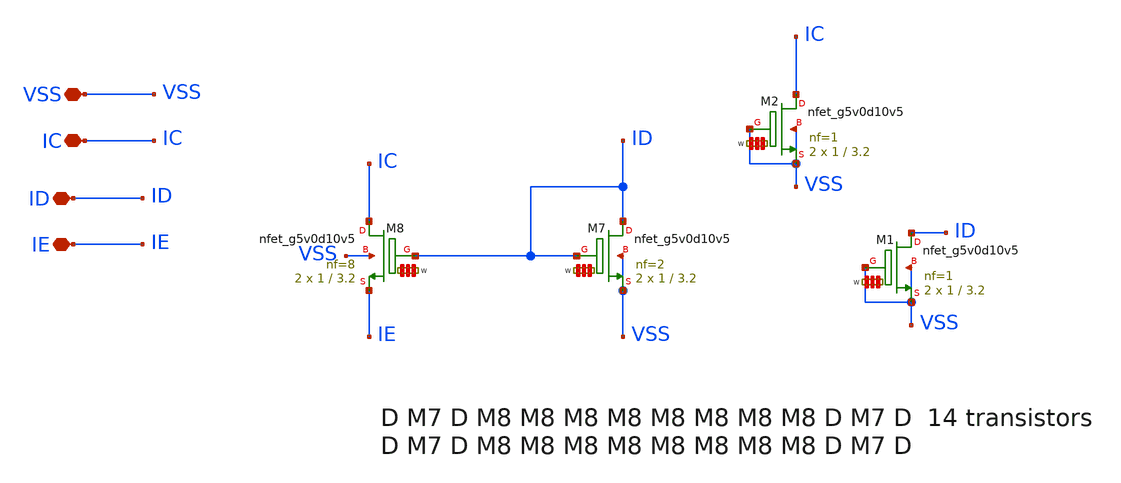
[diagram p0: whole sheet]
** sch_path: Learning/single_ended_amplifiers/Design_and_Analysis_of_Two-Stage_CMOS_Operational_Amplifier_for_Fluorescence_Signal_Processing_sky130_5V/layout/Nmos_lower_current_mirror.sch
**.subckt Nmos_lower_current_mirror VSS IC ID IE
*.iopin VSS
*.iopin IC
*.iopin ID
*.iopin IE
XM7 ID ID VSS VSS sky130_fd_pr__nfet_g5v0d10v5 L=3.2 W='1 * 2 ' nf=2 ad='int((nf+1)/2) * W / nf * 0.29'
+ as='int((nf+2)/2) * W / nf * 0.29' pd='2*int((nf+1)/2) * (W / nf + 0.29)' ps='2*int((nf+2)/2) * (W / nf + 0.29)'
+ nrd='0.29 / W ' nrs='0.29 / W ' sa=0 sb=0 sd=0 mult=2 m=2
XM8 IC ID IE VSS sky130_fd_pr__nfet_g5v0d10v5 L=3.2 W='1 * 8 ' nf=8 ad='int((nf+1)/2) * W / nf * 0.29'
+ as='int((nf+2)/2) * W / nf * 0.29' pd='2*int((nf+1)/2) * (W / nf + 0.29)' ps='2*int((nf+2)/2) * (W / nf + 0.29)'
+ nrd='0.29 / W ' nrs='0.29 / W ' sa=0 sb=0 sd=0 mult=2 m=2
XM1 ID VSS VSS VSS sky130_fd_pr__nfet_g5v0d10v5 L=3.2 W='1 * 1 ' nf=1 ad='int((nf+1)/2) * W / nf * 0.29'
+ as='int((nf+2)/2) * W / nf * 0.29' pd='2*int((nf+1)/2) * (W / nf + 0.29)' ps='2*int((nf+2)/2) * (W / nf + 0.29)'
+ nrd='0.29 / W ' nrs='0.29 / W ' sa=0 sb=0 sd=0 mult=2 m=2
XM2 IC VSS VSS VSS sky130_fd_pr__nfet_g5v0d10v5 L=3.2 W='1 * 1 ' nf=1 ad='int((nf+1)/2) * W / nf * 0.29'
+ as='int((nf+2)/2) * W / nf * 0.29' pd='2*int((nf+1)/2) * (W / nf + 0.29)' ps='2*int((nf+2)/2) * (W / nf + 0.29)'
+ nrd='0.29 / W ' nrs='0.29 / W ' sa=0 sb=0 sd=0 mult=2 m=2
**.ends
.end
